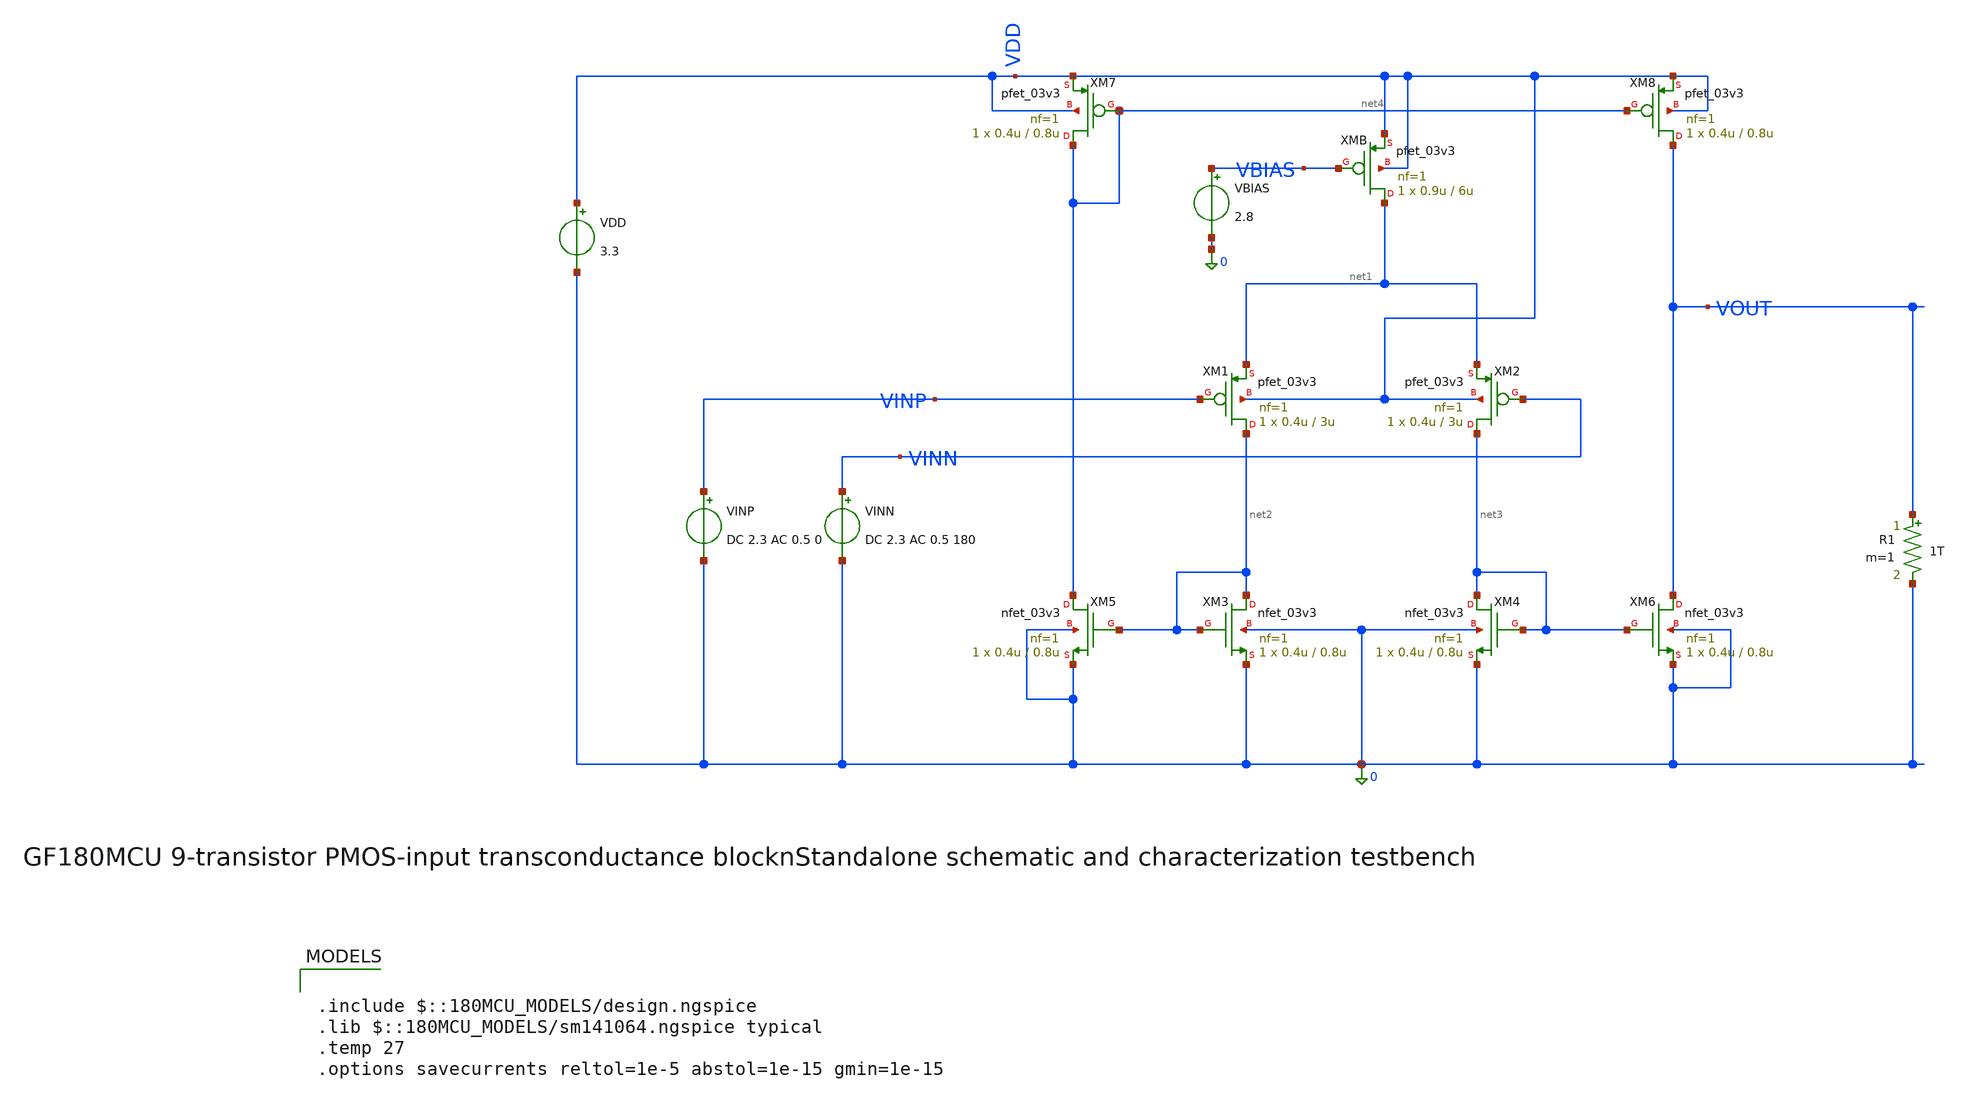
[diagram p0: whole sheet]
** sch_path: gf180_9T_transconductance_DC_AC_TRAN_NOISE.sch
**.subckt gf180_9T_transconductance_DC_AC_TRAN_NOISE
XM1 net2 VINP net1 VDD pfet_03v3 L=3u W=0.4u nf=1 ad='int((nf+1)/2) * W/nf * 0.18u' as='int((nf+2)/2) * W/nf * 0.18u'
+ pd='2*int((nf+1)/2) * (W/nf + 0.18u)' ps='2*int((nf+2)/2) * (W/nf + 0.18u)' nrd='0.18u / W' nrs='0.18u / W'
+ sa=0 sb=0 sd=0 m=1
XM2 net3 VINN net1 VDD pfet_03v3 L=3u W=0.4u nf=1 ad='int((nf+1)/2) * W/nf * 0.18u' as='int((nf+2)/2) * W/nf * 0.18u'
+ pd='2*int((nf+1)/2) * (W/nf + 0.18u)' ps='2*int((nf+2)/2) * (W/nf + 0.18u)' nrd='0.18u / W' nrs='0.18u / W'
+ sa=0 sb=0 sd=0 m=1
XMB net1 VBIAS VDD VDD pfet_03v3 L=6u W=0.9u nf=1 ad='int((nf+1)/2) * W/nf * 0.18u' as='int((nf+2)/2) * W/nf * 0.18u'
+ pd='2*int((nf+1)/2) * (W/nf + 0.18u)' ps='2*int((nf+2)/2) * (W/nf + 0.18u)' nrd='0.18u / W' nrs='0.18u / W'
+ sa=0 sb=0 sd=0 m=1
XM3 net2 net2 0 0 nfet_03v3 L=0.8u W=0.4u nf=1 ad='int((nf+1)/2) * W/nf * 0.18u' as='int((nf+2)/2) * W/nf * 0.18u'
+ pd='2*int((nf+1)/2) * (W/nf + 0.18u)' ps='2*int((nf+2)/2) * (W/nf + 0.18u)' nrd='0.18u / W' nrs='0.18u / W'
+ sa=0 sb=0 sd=0 m=1
XM4 net3 net3 0 0 nfet_03v3 L=0.8u W=0.4u nf=1 ad='int((nf+1)/2) * W/nf * 0.18u' as='int((nf+2)/2) * W/nf * 0.18u'
+ pd='2*int((nf+1)/2) * (W/nf + 0.18u)' ps='2*int((nf+2)/2) * (W/nf + 0.18u)' nrd='0.18u / W' nrs='0.18u / W'
+ sa=0 sb=0 sd=0 m=1
XM7 net4 net4 VDD VDD pfet_03v3 L=0.8u W=0.4u nf=1 ad='int((nf+1)/2) * W/nf * 0.18u' as='int((nf+2)/2) * W/nf * 0.18u'
+ pd='2*int((nf+1)/2) * (W/nf + 0.18u)' ps='2*int((nf+2)/2) * (W/nf + 0.18u)' nrd='0.18u / W' nrs='0.18u / W'
+ sa=0 sb=0 sd=0 m=1
XM5 net4 net2 0 0 nfet_03v3 L=0.8u W=0.4u nf=1 ad='int((nf+1)/2) * W/nf * 0.18u' as='int((nf+2)/2) * W/nf * 0.18u'
+ pd='2*int((nf+1)/2) * (W/nf + 0.18u)' ps='2*int((nf+2)/2) * (W/nf + 0.18u)' nrd='0.18u / W' nrs='0.18u / W'
+ sa=0 sb=0 sd=0 m=1
XM8 VOUT net4 VDD VDD pfet_03v3 L=0.8u W=0.4u nf=1 ad='int((nf+1)/2) * W/nf * 0.18u' as='int((nf+2)/2) * W/nf * 0.18u'
+ pd='2*int((nf+1)/2) * (W/nf + 0.18u)' ps='2*int((nf+2)/2) * (W/nf + 0.18u)' nrd='0.18u / W' nrs='0.18u / W'
+ sa=0 sb=0 sd=0 m=1
XM6 VOUT net3 0 0 nfet_03v3 L=0.8u W=0.4u nf=1 ad='int((nf+1)/2) * W/nf * 0.18u' as='int((nf+2)/2) * W/nf * 0.18u'
+ pd='2*int((nf+1)/2) * (W/nf + 0.18u)' ps='2*int((nf+2)/2) * (W/nf + 0.18u)' nrd='0.18u / W' nrs='0.18u / W'
+ sa=0 sb=0 sd=0 m=1
VDD VDD 0 3.3
.save i(vdd)
VBIAS VBIAS 0 2.8
.save i(vbias)
VINP VINP 0 DC 2.3 AC 0.5 0
.save i(vinp)
VINN VINN 0 DC 2.3 AC 0.5 180
.save i(vinn)
R1 VOUT 0 1T m=1
**** begin user architecture code

.include $::180MCU_MODELS/design.ngspice
.lib $::180MCU_MODELS/sm141064.ngspice typical
.temp 27
.options savecurrents reltol=1e-5 abstol=1e-15 gmin=1e-15



.control
save all

op

ac dec 100 0.1 10Meg

let vid = v(vinp)-v(vinn)
let av = v(vout)/vid

let gain_db = db(av)
let phase_deg = 180/pi*cph(av)

plot gain_db xlog
plot phase_deg xlog

meas ac gain_1hz find gain_db at=1
meas ac gain_10hz find gain_db at=10
meas ac ugf when gain_db=0 fall=1

print gain_1hz
print gain_10hz
print ugf

.endc


**** end user architecture code
**.ends
.end
